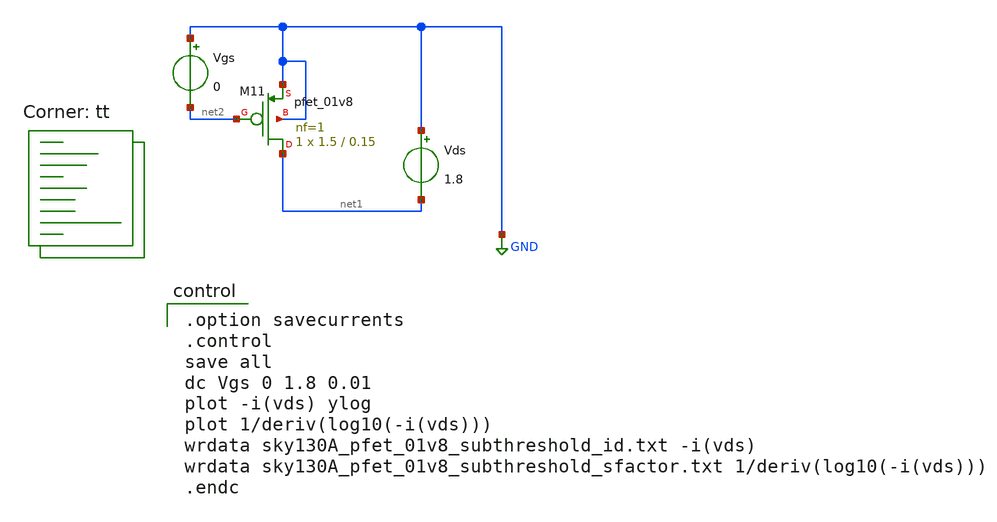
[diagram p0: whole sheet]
** sch_path: xschem/MOSFET/sky130A_pfet_01v8_subthreshold.sch
**.subckt sky130A_pfet_01v8_subthreshold
Vgs GND net2 0
Vds GND net1 1.8
XM11 net1 net2 GND GND sky130_fd_pr__pfet_01v8 L=0.15 W=1.5 nf=1 ad='int((nf+1)/2) * W/nf * 0.29' as='int((nf+2)/2) * W/nf * 0.29'
+ pd='2*int((nf+1)/2) * (W/nf + 0.29)' ps='2*int((nf+2)/2) * (W/nf + 0.29)' nrd='0.29 / W' nrs='0.29 / W'
+ sa=0 sb=0 sd=0 mult=1 m=1
**** begin user architecture code

.option savecurrents
.control
save all
dc Vgs 0 1.8 0.01
plot -i(vds) ylog
plot 1/deriv(log10(-i(vds)))
wrdata sky130A_pfet_01v8_subthreshold_id.txt -i(vds)
wrdata sky130A_pfet_01v8_subthreshold_sfactor.txt 1/deriv(log10(-i(vds)))
.endc

.lib $::SKYWATER_MODELS/sky130.lib.spice tt
**** end user architecture code
**.ends
.GLOBAL GND
.end
